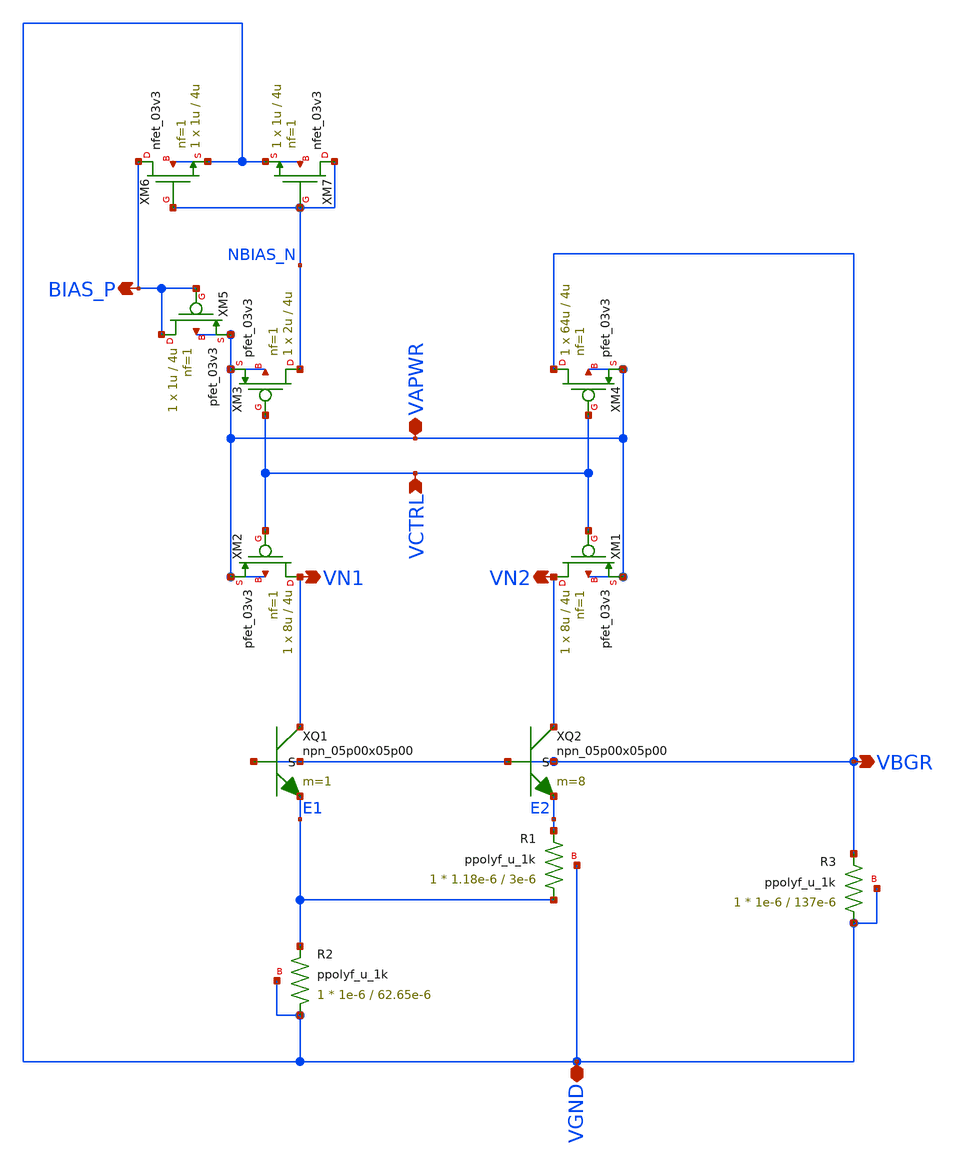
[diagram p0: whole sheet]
** sch_path: xschem/bgr_core_without_amp.sch
**.subckt bgr_core_without_amp VGND VAPWR VBGR VCTRL BIAS_P VN1 VN2
*.iopin VGND
*.iopin VAPWR
*.opin VBGR
*.ipin VCTRL
*.opin BIAS_P
*.opin VN1
*.opin VN2
XQ1 VN1 VBGR E1 VBGR npn_05p00x05p00 m=1
XQ2 VN2 VBGR E2 VBGR npn_05p00x05p00 m=8
XR1 E1 E2 VGND ppolyf_u_1k r_width=1.18e-6 r_length=3e-6 m=1
XR2 VGND E1 VGND ppolyf_u_1k r_width=1e-6 r_length=62.65e-6 m=1
XR3 VGND VBGR VGND ppolyf_u_1k r_width=1e-6 r_length=137e-6 m=1
XM1 VN2 VCTRL VAPWR VAPWR pfet_03v3 L=4u W=8u nf=1 ad='int((nf+1)/2) * W/nf * 0.18u' as='int((nf+2)/2) * W/nf * 0.18u'
+ pd='2*int((nf+1)/2) * (W/nf + 0.18u)' ps='2*int((nf+2)/2) * (W/nf + 0.18u)' nrd='0.18u / W' nrs='0.18u / W'
+ sa=0 sb=0 sd=0 m=1
XM2 VN1 VCTRL VAPWR VAPWR pfet_03v3 L=4u W=8u nf=1 ad='int((nf+1)/2) * W/nf * 0.18u' as='int((nf+2)/2) * W/nf * 0.18u'
+ pd='2*int((nf+1)/2) * (W/nf + 0.18u)' ps='2*int((nf+2)/2) * (W/nf + 0.18u)' nrd='0.18u / W' nrs='0.18u / W'
+ sa=0 sb=0 sd=0 m=1
XM3 NBIAS_N VCTRL VAPWR VAPWR pfet_03v3 L=4u W=2u nf=1 ad='int((nf+1)/2) * W/nf * 0.18u' as='int((nf+2)/2) * W/nf * 0.18u'
+ pd='2*int((nf+1)/2) * (W/nf + 0.18u)' ps='2*int((nf+2)/2) * (W/nf + 0.18u)' nrd='0.18u / W' nrs='0.18u / W'
+ sa=0 sb=0 sd=0 m=1
XM4 VBGR VCTRL VAPWR VAPWR pfet_03v3 L=4u W=64u nf=1 ad='int((nf+1)/2) * W/nf * 0.18u' as='int((nf+2)/2) * W/nf * 0.18u'
+ pd='2*int((nf+1)/2) * (W/nf + 0.18u)' ps='2*int((nf+2)/2) * (W/nf + 0.18u)' nrd='0.18u / W' nrs='0.18u / W'
+ sa=0 sb=0 sd=0 m=1
XM5 BIAS_P BIAS_P VAPWR VAPWR pfet_03v3 L=4u W=1u nf=1 ad='int((nf+1)/2) * W/nf * 0.18u' as='int((nf+2)/2) * W/nf * 0.18u'
+ pd='2*int((nf+1)/2) * (W/nf + 0.18u)' ps='2*int((nf+2)/2) * (W/nf + 0.18u)' nrd='0.18u / W' nrs='0.18u / W'
+ sa=0 sb=0 sd=0 m=1
XM6 BIAS_P NBIAS_N VGND VGND nfet_03v3 L=4u W=1u nf=1 ad='int((nf+1)/2) * W/nf * 0.18u' as='int((nf+2)/2) * W/nf * 0.18u'
+ pd='2*int((nf+1)/2) * (W/nf + 0.18u)' ps='2*int((nf+2)/2) * (W/nf + 0.18u)' nrd='0.18u / W' nrs='0.18u / W'
+ sa=0 sb=0 sd=0 m=1
XM7 NBIAS_N NBIAS_N VGND VGND nfet_03v3 L=4u W=1u nf=1 ad='int((nf+1)/2) * W/nf * 0.18u' as='int((nf+2)/2) * W/nf * 0.18u'
+ pd='2*int((nf+1)/2) * (W/nf + 0.18u)' ps='2*int((nf+2)/2) * (W/nf + 0.18u)' nrd='0.18u / W' nrs='0.18u / W'
+ sa=0 sb=0 sd=0 m=1
**.ends
.end
